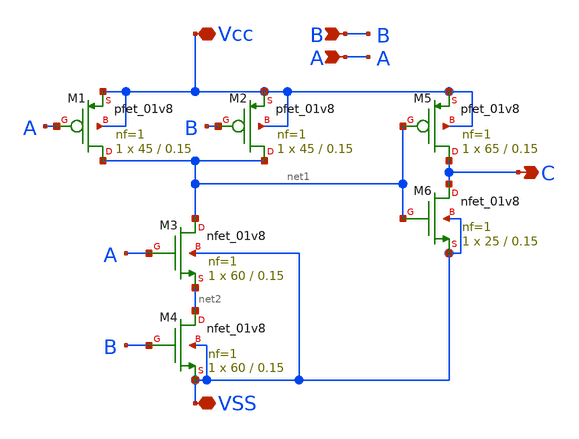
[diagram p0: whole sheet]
** sch_path: Git Files/Schematic/Pre Emphasis Driver/and.sch
**.subckt and C Vcc VSS A B
*.opin C
*.iopin Vcc
*.iopin VSS
*.ipin A
*.ipin B
XM1 net1 A Vcc Vcc sky130_fd_pr__pfet_01v8 L=0.15 W=45 nf=1 ad='int((nf+1)/2) * W/nf * 0.29' as='int((nf+2)/2) * W/nf * 0.29'
+ pd='2*int((nf+1)/2) * (W/nf + 0.29)' ps='2*int((nf+2)/2) * (W/nf + 0.29)' nrd='0.29 / W' nrs='0.29 / W'
+ sa=0 sb=0 sd=0 mult=1 m=1
XM2 net1 B Vcc Vcc sky130_fd_pr__pfet_01v8 L=0.15 W=45 nf=1 ad='int((nf+1)/2) * W/nf * 0.29' as='int((nf+2)/2) * W/nf * 0.29'
+ pd='2*int((nf+1)/2) * (W/nf + 0.29)' ps='2*int((nf+2)/2) * (W/nf + 0.29)' nrd='0.29 / W' nrs='0.29 / W'
+ sa=0 sb=0 sd=0 mult=1 m=1
XM3 net1 A net2 VSS sky130_fd_pr__nfet_01v8 L=0.15 W=60 nf=1 ad='int((nf+1)/2) * W/nf * 0.29' as='int((nf+2)/2) * W/nf * 0.29'
+ pd='2*int((nf+1)/2) * (W/nf + 0.29)' ps='2*int((nf+2)/2) * (W/nf + 0.29)' nrd='0.29 / W' nrs='0.29 / W'
+ sa=0 sb=0 sd=0 mult=1 m=1
XM4 net2 B VSS VSS sky130_fd_pr__nfet_01v8 L=0.15 W=60 nf=1 ad='int((nf+1)/2) * W/nf * 0.29' as='int((nf+2)/2) * W/nf * 0.29'
+ pd='2*int((nf+1)/2) * (W/nf + 0.29)' ps='2*int((nf+2)/2) * (W/nf + 0.29)' nrd='0.29 / W' nrs='0.29 / W'
+ sa=0 sb=0 sd=0 mult=1 m=1
XM5 C net1 Vcc Vcc sky130_fd_pr__pfet_01v8 L=0.15 W=65 nf=1 ad='int((nf+1)/2) * W/nf * 0.29' as='int((nf+2)/2) * W/nf * 0.29'
+ pd='2*int((nf+1)/2) * (W/nf + 0.29)' ps='2*int((nf+2)/2) * (W/nf + 0.29)' nrd='0.29 / W' nrs='0.29 / W'
+ sa=0 sb=0 sd=0 mult=1 m=1
XM6 C net1 VSS VSS sky130_fd_pr__nfet_01v8 L=0.15 W=25 nf=1 ad='int((nf+1)/2) * W/nf * 0.29' as='int((nf+2)/2) * W/nf * 0.29'
+ pd='2*int((nf+1)/2) * (W/nf + 0.29)' ps='2*int((nf+2)/2) * (W/nf + 0.29)' nrd='0.29 / W' nrs='0.29 / W'
+ sa=0 sb=0 sd=0 mult=1 m=1
**.ends
.end
